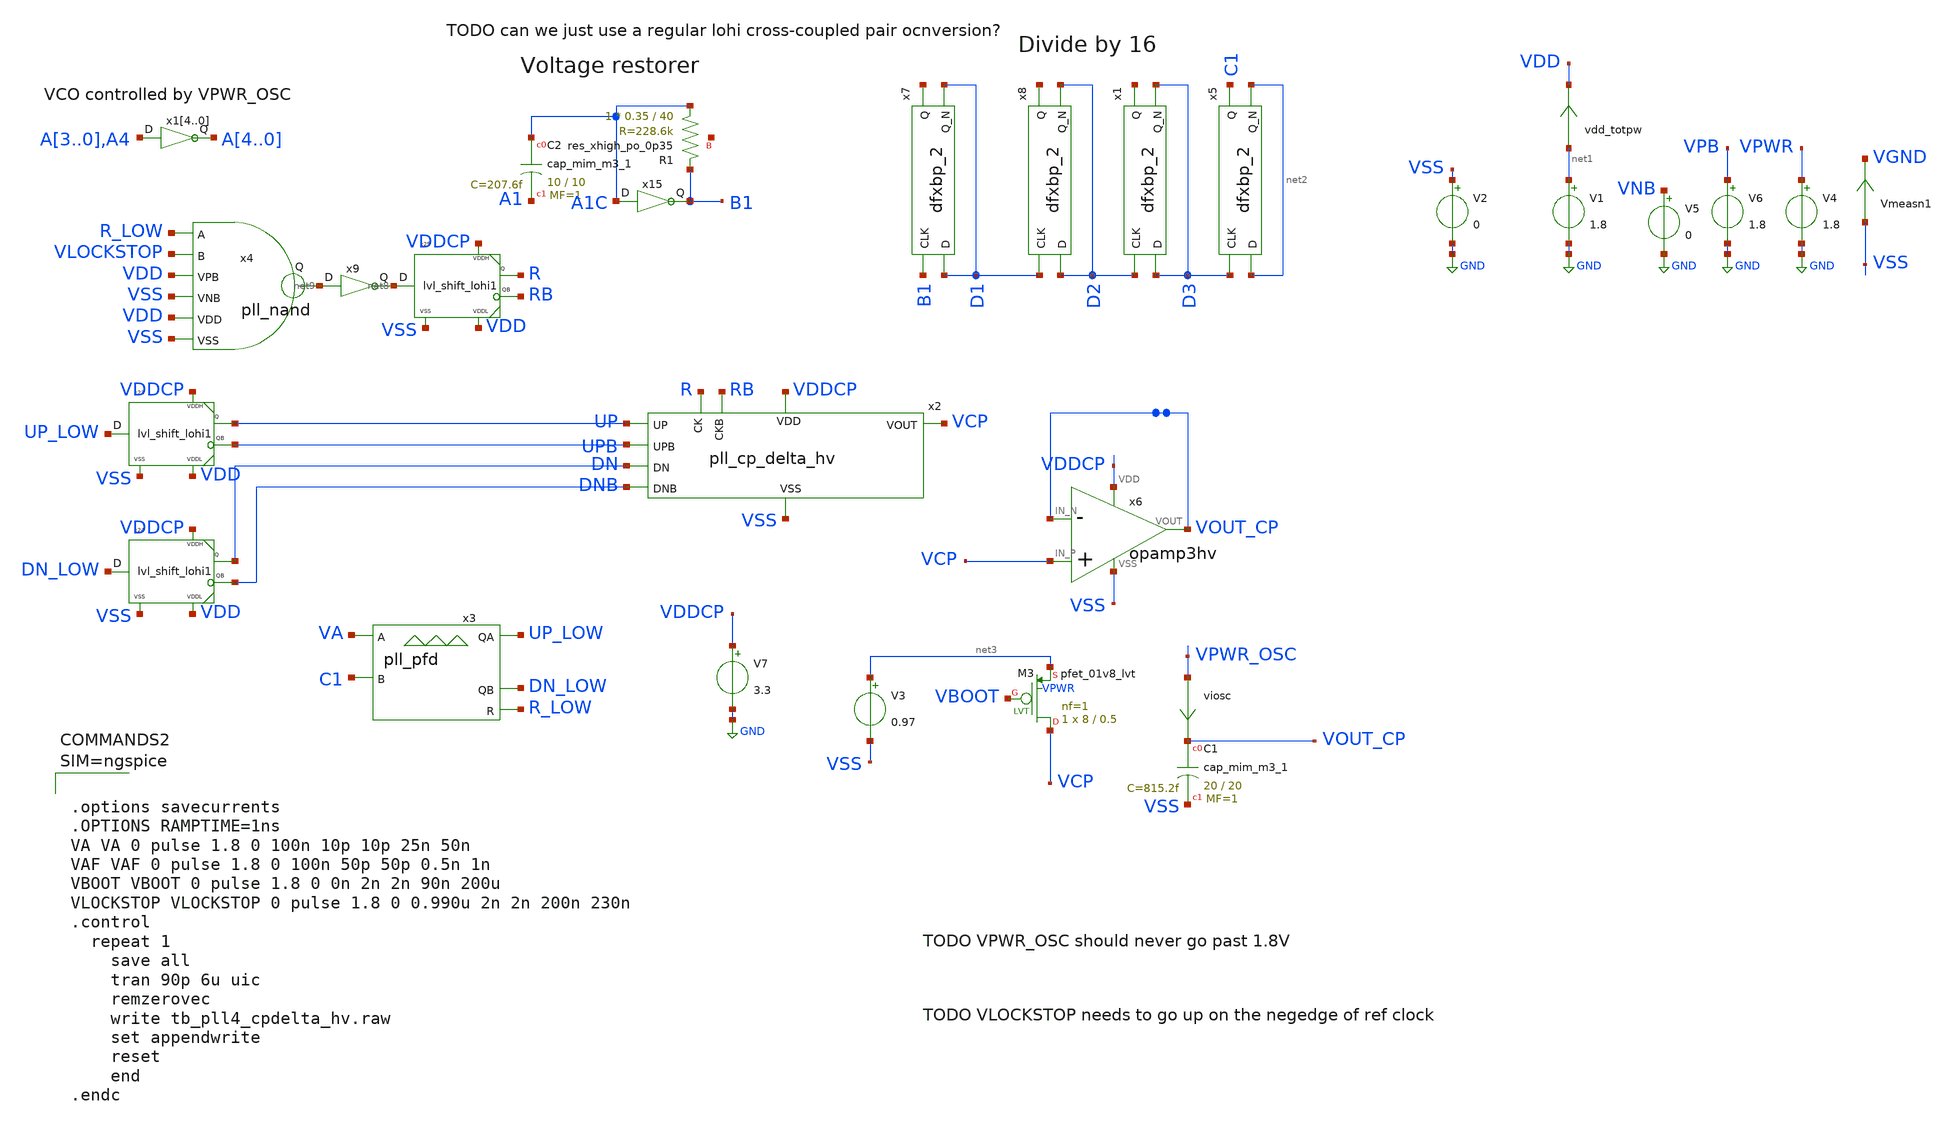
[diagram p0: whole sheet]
** sch_path: xschem/tb_pll4_cpdelta_hv.sch
**.subckt tb_pll4_cpdelta_hv
V5 VNB GND 0
V6 VPB GND 1.8
V1 net1 GND 1.8
V2 VSS GND 0
vdd_totpw net1 VDD 0
.save i(vdd_totpw)
Vmeasn1 VSS VGND 0
.save i(vmeasn1)
x3 VA C1 UP_LOW DN_LOW R_LOW VDD VSS pll_pfd
x7 B1 D1 VGND VNB VPB VPWR net4 D1 sky130_fd_sc_hd__dfxbp_2
x8 D1 D2 VGND VNB VPB VPWR net5 D2 sky130_fd_sc_hd__dfxbp_2
V4 VPWR GND 1.8
x1 D2 D3 VGND VNB VPB VPWR net6 D3 sky130_fd_sc_hd__dfxbp_2
x5 D3 net2 VGND VNB VPB VPWR C1 net2 sky130_fd_sc_hd__dfxbp_2
x14 A3 A4 VPWR_OSC VSS pll_inv1
x13 A2 A3 VPWR_OSC VSS pll_inv1
x12 A1 A2 VPWR_OSC VSS pll_inv1
x11 A0 A1 VPWR_OSC VSS pll_inv1
x10 A4 A0 VPWR_OSC VSS pll_inv1
V7 VDDCP GND 3.3
x15 A1C B1 VDD VSS pll_inv1
XR1 A1C B1 net7 sky130_fd_pr__res_xhigh_po_0p35 L=40 mult=1 m=1
XC2 A1C A1 sky130_fd_pr__cap_mim_m3_1 W=10 L=10 MF=1 m=1
viosc VPWR_OSC VOUT_CP 0
.save i(viosc)
V3 net3 VSS 0.97
x6 VDDCP VCP VOUT_CP VOUT_CP VSS opamp3hv
x2 VDDCP UP DN VCP VSS UPB DNB R RB pll_cp_delta_hv
x23 UP_LOW UP UPB VDDCP VDD VSS lvl_shift_lohi1
x24 DN_LOW DN DNB VDDCP VDD VSS lvl_shift_lohi1
x25 net8 R RB VDDCP VDD VSS lvl_shift_lohi1
x4 R_LOW VLOCKSTOP VDD VSS VDD VSS net9 pll_nand
x9 net9 net8 VDD VSS pll_inv1
XC1 VOUT_CP VSS sky130_fd_pr__cap_mim_m3_1 W=20 L=20 MF=1 m=1
XM3 VCP VBOOT net3 VPWR sky130_fd_pr__pfet_01v8_lvt L=0.5 W=8 nf=1 ad='int((nf+1)/2) * W/nf * 0.29' as='int((nf+2)/2) * W/nf * 0.29'
+ pd='2*int((nf+1)/2) * (W/nf + 0.29)' ps='2*int((nf+2)/2) * (W/nf + 0.29)' nrd='0.29 / W' nrs='0.29 / W'
+ sa=0 sb=0 sd=0 mult=1 m=1
**** begin user architecture code

** opencircuitdesign pdks install
.lib $::SKYWATER_MODELS/sky130.lib.spice tt_mm
.include $::SKYWATER_STDCELLS/sky130_fd_sc_hd.spice





.options savecurrents
.OPTIONS RAMPTIME=1ns
VA VA 0 pulse 1.8 0 100n 10p 10p 25n 50n
VAF VAF 0 pulse 1.8 0 100n 50p 50p 0.5n 1n
VBOOT VBOOT 0 pulse 1.8 0 0n 2n 2n 90n 200u
VLOCKSTOP VLOCKSTOP 0 pulse 1.8 0 0.990u 2n 2n 200n 230n
.control
  repeat 1
    save all
    tran 90p 6u uic
    remzerovec
    write tb_pll4_cpdelta_hv.raw
    set appendwrite
    reset
    end
.endc



**** end user architecture code
**.ends

* expanding   symbol:  pll_pfd.sym # of pins=5
** sym_path: xschem/pll_pfd.sym
** sch_path: xschem/pll_pfd.sch
.subckt pll_pfd A B QA QB R VDD VSS
*.ipin A
*.ipin B
*.iopin VDD
*.ipin VSS
*.opin QA
*.opin QB
*.opin R
x1 QA A QAB VDD VSS pll_nor
x2 QAB RA QA VDD VSS pll_nor
x3 QB B QBB VDD VSS pll_nor
x4 QBB RB QB VDD VSS pll_nor
x6 RAB QAB RA VDD VSS pll_nor
x7 RA R RAB VDD VSS pll_nor
x8 RBB QBB RB VDD VSS pll_nor
x9 RB R RBB VDD VSS pll_nor
x10 net2 net1 VDD VSS pll_inv1
x11 net3 net2 VDD VSS pll_inv1
x12 net1 R VDD VSS pll_inv1
x13 net1 R VDD VSS pll_inv1
x14 net1 R VDD VSS pll_inv1
x15 QB QA net3 VDD VSS pll_nand
.ends


* expanding   symbol:  pll_inv1.sym # of pins=2
** sym_path: xschem/pll_inv1.sym
** sch_path: xschem/pll_inv1.sch
.subckt pll_inv1 D Q VDD VSS
*.opin Q
*.ipin D
*.ipin VDD
*.ipin VSS
XM3 Q D net1 net1 sky130_fd_pr__pfet_01v8_lvt L=0.5 W=1 nf=1 ad='int((nf+1)/2) * W/nf * 0.29' as='int((nf+2)/2) * W/nf * 0.29'
+ pd='2*int((nf+1)/2) * (W/nf + 0.29)' ps='2*int((nf+2)/2) * (W/nf + 0.29)' nrd='0.29 / W' nrs='0.29 / W'
+ sa=0 sb=0 sd=0 mult=1 m=1
vpwr VDD net1 0
.save i(vpwr)
XM1 Q D VSS VSS sky130_fd_pr__nfet_01v8_lvt L=0.25 W=0.5 nf=1 ad='int((nf+1)/2) * W/nf * 0.29' as='int((nf+2)/2) * W/nf * 0.29'
+ pd='2*int((nf+1)/2) * (W/nf + 0.29)' ps='2*int((nf+2)/2) * (W/nf + 0.29)' nrd='0.29 / W' nrs='0.29 / W'
+ sa=0 sb=0 sd=0 mult=1 m=1
.ends


* expanding   symbol:  opamp3hv.sym # of pins=5
** sym_path: xschem/opamp3hv.sym
** sch_path: xschem/opamp3hv.sch
.subckt opamp3hv VDD IN_P IN_N VOUT VSS
*.iopin VDD
*.iopin VSS
*.ipin IN_N
*.opin VOUT
*.ipin IN_P
vimeasn net2 VN 0
.save i(vimeasn)
vimeasp net3 voutstage1 0
.save i(vimeasp)
vicom vcom net1 0
.save i(vicom)
V3 vbias VSS 1.2
XC1 VOUT voutstage1 sky130_fd_pr__cap_mim_m3_1 W=8 L=8 MF=1 m=1
XM6 net1 vbias VSS VSS sky130_fd_pr__nfet_g5v0d10v5 L=1 W=2 nf=1 ad='int((nf+1)/2) * W/nf * 0.29' as='int((nf+2)/2) * W/nf * 0.29'
+ pd='2*int((nf+1)/2) * (W/nf + 0.29)' ps='2*int((nf+2)/2) * (W/nf + 0.29)' nrd='0.29 / W' nrs='0.29 / W'
+ sa=0 sb=0 sd=0 mult=1 m=1
XM7 VN IN_N vcom VSS sky130_fd_pr__nfet_g5v0d10v5 L=1 W=2 nf=1 ad='int((nf+1)/2) * W/nf * 0.29' as='int((nf+2)/2) * W/nf * 0.29'
+ pd='2*int((nf+1)/2) * (W/nf + 0.29)' ps='2*int((nf+2)/2) * (W/nf + 0.29)' nrd='0.29 / W' nrs='0.29 / W'
+ sa=0 sb=0 sd=0 mult=1 m=1
XM8 net3 net2 VDD VDD sky130_fd_pr__pfet_g5v0d10v5 L=1 W=2 nf=1 ad='int((nf+1)/2) * W/nf * 0.29' as='int((nf+2)/2) * W/nf * 0.29'
+ pd='2*int((nf+1)/2) * (W/nf + 0.29)' ps='2*int((nf+2)/2) * (W/nf + 0.29)' nrd='0.29 / W' nrs='0.29 / W'
+ sa=0 sb=0 sd=0 mult=1 m=1
XM2 net2 net2 VDD VDD sky130_fd_pr__pfet_g5v0d10v5 L=1 W=2 nf=1 ad='int((nf+1)/2) * W/nf * 0.29' as='int((nf+2)/2) * W/nf * 0.29'
+ pd='2*int((nf+1)/2) * (W/nf + 0.29)' ps='2*int((nf+2)/2) * (W/nf + 0.29)' nrd='0.29 / W' nrs='0.29 / W'
+ sa=0 sb=0 sd=0 mult=1 m=1
XM1 VOUT voutstage1 VDD VDD sky130_fd_pr__pfet_g5v0d10v5 L=1 W=4 nf=1 ad='int((nf+1)/2) * W/nf * 0.29'
+ as='int((nf+2)/2) * W/nf * 0.29' pd='2*int((nf+1)/2) * (W/nf + 0.29)' ps='2*int((nf+2)/2) * (W/nf + 0.29)'
+ nrd='0.29 / W' nrs='0.29 / W' sa=0 sb=0 sd=0 mult=1 m=1
XM4 VOUT vbias VSS VSS sky130_fd_pr__nfet_g5v0d10v5 L=1 W=2 nf=1 ad='int((nf+1)/2) * W/nf * 0.29' as='int((nf+2)/2) * W/nf * 0.29'
+ pd='2*int((nf+1)/2) * (W/nf + 0.29)' ps='2*int((nf+2)/2) * (W/nf + 0.29)' nrd='0.29 / W' nrs='0.29 / W'
+ sa=0 sb=0 sd=0 mult=1 m=1
XM9 voutstage1 IN_P vcom VSS sky130_fd_pr__nfet_g5v0d10v5 L=1 W=2 nf=1 ad='int((nf+1)/2) * W/nf * 0.29'
+ as='int((nf+2)/2) * W/nf * 0.29' pd='2*int((nf+1)/2) * (W/nf + 0.29)' ps='2*int((nf+2)/2) * (W/nf + 0.29)'
+ nrd='0.29 / W' nrs='0.29 / W' sa=0 sb=0 sd=0 mult=1 m=1
.ends


* expanding   symbol:  pll_cp_delta_hv.sym # of pins=9
** sym_path: xschem/pll_cp_delta_hv.sym
** sch_path: xschem/pll_cp_delta_hv.sch
.subckt pll_cp_delta_hv VDD UP DN VOUT VSS UPB DNB CK CKB
*.opin VOUT
*.ipin VSS
*.ipin UP
*.ipin DNB
*.ipin CK
*.ipin CKB
*.ipin VDD
*.ipin DN
*.ipin UPB
*.ipin CK
vibias net3 net9 0
.save i(vibias)
XM16 net6 UPB VDD VDD sky130_fd_pr__pfet_g5v0d10v5 L=1 W=4 nf=1 ad='int((nf+1)/2) * W/nf * 0.29' as='int((nf+2)/2) * W/nf * 0.29'
+ pd='2*int((nf+1)/2) * (W/nf + 0.29)' ps='2*int((nf+2)/2) * (W/nf + 0.29)' nrd='0.29 / W' nrs='0.29 / W'
+ sa=0 sb=0 sd=0 mult=1 m=1
XM13 net2 VSS VDD VDD sky130_fd_pr__pfet_g5v0d10v5 L=1 W=4 nf=1 ad='int((nf+1)/2) * W/nf * 0.29' as='int((nf+2)/2) * W/nf * 0.29'
+ pd='2*int((nf+1)/2) * (W/nf + 0.29)' ps='2*int((nf+2)/2) * (W/nf + 0.29)' nrd='0.29 / W' nrs='0.29 / W'
+ sa=0 sb=0 sd=0 mult=1 m=1
XM14 net3 net3 net2 VDD sky130_fd_pr__pfet_g5v0d10v5 L=1 W=4 nf=1 ad='int((nf+1)/2) * W/nf * 0.29' as='int((nf+2)/2) * W/nf * 0.29'
+ pd='2*int((nf+1)/2) * (W/nf + 0.29)' ps='2*int((nf+2)/2) * (W/nf + 0.29)' nrd='0.29 / W' nrs='0.29 / W'
+ sa=0 sb=0 sd=0 mult=1 m=1
I0 VDD net4 10u
XM11 net1 VDD VSS VSS sky130_fd_pr__nfet_g5v0d10v5 L=1 W=2 nf=1 ad='int((nf+1)/2) * W/nf * 0.29' as='int((nf+2)/2) * W/nf * 0.29'
+ pd='2*int((nf+1)/2) * (W/nf + 0.29)' ps='2*int((nf+2)/2) * (W/nf + 0.29)' nrd='0.29 / W' nrs='0.29 / W'
+ sa=0 sb=0 sd=0 mult=1 m=1
XM17 net4 net4 net1 VSS sky130_fd_pr__nfet_g5v0d10v5 L=1 W=2 nf=1 ad='int((nf+1)/2) * W/nf * 0.29' as='int((nf+2)/2) * W/nf * 0.29'
+ pd='2*int((nf+1)/2) * (W/nf + 0.29)' ps='2*int((nf+2)/2) * (W/nf + 0.29)' nrd='0.29 / W' nrs='0.29 / W'
+ sa=0 sb=0 sd=0 mult=1 m=1
XM15 net5 VDD VSS VSS sky130_fd_pr__nfet_g5v0d10v5 L=1 W=2 nf=1 ad='int((nf+1)/2) * W/nf * 0.29' as='int((nf+2)/2) * W/nf * 0.29'
+ pd='2*int((nf+1)/2) * (W/nf + 0.29)' ps='2*int((nf+2)/2) * (W/nf + 0.29)' nrd='0.29 / W' nrs='0.29 / W'
+ sa=0 sb=0 sd=0 mult=1 m=1
XM18 net9 net4 net5 VSS sky130_fd_pr__nfet_g5v0d10v5 L=1 W=2 nf=1 ad='int((nf+1)/2) * W/nf * 0.29' as='int((nf+2)/2) * W/nf * 0.29'
+ pd='2*int((nf+1)/2) * (W/nf + 0.29)' ps='2*int((nf+2)/2) * (W/nf + 0.29)' nrd='0.29 / W' nrs='0.29 / W'
+ sa=0 sb=0 sd=0 mult=1 m=1
XM6 net7 DN VSS VSS sky130_fd_pr__nfet_g5v0d10v5 L=1 W=2 nf=1 ad='int((nf+1)/2) * W/nf * 0.29' as='int((nf+2)/2) * W/nf * 0.29'
+ pd='2*int((nf+1)/2) * (W/nf + 0.29)' ps='2*int((nf+2)/2) * (W/nf + 0.29)' nrd='0.29 / W' nrs='0.29 / W'
+ sa=0 sb=0 sd=0 mult=1 m=1
XM19 net8 net4 net7 VSS sky130_fd_pr__nfet_g5v0d10v5 L=1 W=2 nf=1 ad='int((nf+1)/2) * W/nf * 0.29' as='int((nf+2)/2) * W/nf * 0.29'
+ pd='2*int((nf+1)/2) * (W/nf + 0.29)' ps='2*int((nf+2)/2) * (W/nf + 0.29)' nrd='0.29 / W' nrs='0.29 / W'
+ sa=0 sb=0 sd=0 mult=1 m=1
XM4 net10 net3 net6 VDD sky130_fd_pr__pfet_g5v0d10v5 L=1 W=4 nf=1 ad='int((nf+1)/2) * W/nf * 0.29' as='int((nf+2)/2) * W/nf * 0.29'
+ pd='2*int((nf+1)/2) * (W/nf + 0.29)' ps='2*int((nf+2)/2) * (W/nf + 0.29)' nrd='0.29 / W' nrs='0.29 / W'
+ sa=0 sb=0 sd=0 mult=1 m=1
viup net10 VOUT 0
.save i(viup)
vidown VOUT net8 0
.save i(vidown)
XC3 VOUT VOUT sky130_fd_pr__cap_mim_m3_1 W=1 L=1 MF=1 m=1
XM3 VOUT CKB VOUT VDD sky130_fd_pr__pfet_01v8_lvt L=0.5 W=1 nf=1 ad='int((nf+1)/2) * W/nf * 0.29' as='int((nf+2)/2) * W/nf * 0.29'
+ pd='2*int((nf+1)/2) * (W/nf + 0.29)' ps='2*int((nf+2)/2) * (W/nf + 0.29)' nrd='0.29 / W' nrs='0.29 / W'
+ sa=0 sb=0 sd=0 mult=1 m=1
XM5 VOUT CK VOUT VSS sky130_fd_pr__nfet_01v8_lvt L=0.25 W=0.45 nf=1 ad='int((nf+1)/2) * W/nf * 0.29'
+ as='int((nf+2)/2) * W/nf * 0.29' pd='2*int((nf+1)/2) * (W/nf + 0.29)' ps='2*int((nf+2)/2) * (W/nf + 0.29)'
+ nrd='0.29 / W' nrs='0.29 / W' sa=0 sb=0 sd=0 mult=1 m=1
XC2 VOUT VSS sky130_fd_pr__cap_mim_m3_1 W=1500 L=150 MF=1 m=1
.ends


* expanding   symbol:  lvl_shift_lohi1.sym # of pins=6
** sym_path: xschem/lvl_shift_lohi1.sym
** sch_path: xschem/lvl_shift_lohi1.sch
.subckt lvl_shift_lohi1 D Q QB VDDH VDDL VSS
*.ipin D
*.opin Q
*.opin QB
*.iopin VDDH
*.iopin VDDL
*.iopin VSS
vpwr VDDL net1 0
.save i(vpwr)
XM1 QB Q VDDH VDDH sky130_fd_pr__pfet_g5v0d10v5 L=0.5 W=2 nf=1 ad='int((nf+1)/2) * W/nf * 0.29' as='int((nf+2)/2) * W/nf * 0.29'
+ pd='2*int((nf+1)/2) * (W/nf + 0.29)' ps='2*int((nf+2)/2) * (W/nf + 0.29)' nrd='0.29 / W' nrs='0.29 / W'
+ sa=0 sb=0 sd=0 mult=1 m=1
XM2 Q QB VDDH VDDH sky130_fd_pr__pfet_g5v0d10v5 L=0.5 W=2 nf=1 ad='int((nf+1)/2) * W/nf * 0.29' as='int((nf+2)/2) * W/nf * 0.29'
+ pd='2*int((nf+1)/2) * (W/nf + 0.29)' ps='2*int((nf+2)/2) * (W/nf + 0.29)' nrd='0.29 / W' nrs='0.29 / W'
+ sa=0 sb=0 sd=0 mult=1 m=1
XM3 QB D VSS VSS sky130_fd_pr__nfet_g5v0d10v5 L=0.5 W=4 nf=1 ad='int((nf+1)/2) * W/nf * 0.29' as='int((nf+2)/2) * W/nf * 0.29'
+ pd='2*int((nf+1)/2) * (W/nf + 0.29)' ps='2*int((nf+2)/2) * (W/nf + 0.29)' nrd='0.29 / W' nrs='0.29 / W'
+ sa=0 sb=0 sd=0 mult=1 m=1
XM4 Q DB VSS VSS sky130_fd_pr__nfet_g5v0d10v5 L=0.5 W=4 nf=1 ad='int((nf+1)/2) * W/nf * 0.29' as='int((nf+2)/2) * W/nf * 0.29'
+ pd='2*int((nf+1)/2) * (W/nf + 0.29)' ps='2*int((nf+2)/2) * (W/nf + 0.29)' nrd='0.29 / W' nrs='0.29 / W'
+ sa=0 sb=0 sd=0 mult=1 m=1
XM5 DB D VSS VSS sky130_fd_pr__nfet_01v8_lvt L=0.5 W=1 nf=1 ad='int((nf+1)/2) * W/nf * 0.29' as='int((nf+2)/2) * W/nf * 0.29'
+ pd='2*int((nf+1)/2) * (W/nf + 0.29)' ps='2*int((nf+2)/2) * (W/nf + 0.29)' nrd='0.29 / W' nrs='0.29 / W'
+ sa=0 sb=0 sd=0 mult=1 m=1
XM6 DB D net1 VDDL sky130_fd_pr__pfet_01v8_lvt L=0.5 W=2 nf=1 ad='int((nf+1)/2) * W/nf * 0.29' as='int((nf+2)/2) * W/nf * 0.29'
+ pd='2*int((nf+1)/2) * (W/nf + 0.29)' ps='2*int((nf+2)/2) * (W/nf + 0.29)' nrd='0.29 / W' nrs='0.29 / W'
+ sa=0 sb=0 sd=0 mult=1 m=1
.ends


* expanding   symbol:  pll_nand.sym # of pins=7
** sym_path: xschem/pll_nand.sym
** sch_path: xschem/pll_nand.sch
.subckt pll_nand A B VPB VNB VDD VSS Q
*.opin Q
*.ipin A
*.ipin B
*.ipin VDD
*.ipin VPB
*.ipin VNB
*.ipin VSS
XM3 Q B net2 VPB sky130_fd_pr__pfet_01v8_lvt L=0.35 W=1 nf=1 ad='int((nf+1)/2) * W/nf * 0.29' as='int((nf+2)/2) * W/nf * 0.29'
+ pd='2*int((nf+1)/2) * (W/nf + 0.29)' ps='2*int((nf+2)/2) * (W/nf + 0.29)' nrd='0.29 / W' nrs='0.29 / W'
+ sa=0 sb=0 sd=0 mult=1 m=1
vpwr VDD net2 0
.save i(vpwr)
XM1 net1 B VSS VNB sky130_fd_pr__nfet_01v8_lvt L=0.25 W=0.5 nf=1 ad='int((nf+1)/2) * W/nf * 0.29' as='int((nf+2)/2) * W/nf * 0.29'
+ pd='2*int((nf+1)/2) * (W/nf + 0.29)' ps='2*int((nf+2)/2) * (W/nf + 0.29)' nrd='0.29 / W' nrs='0.29 / W'
+ sa=0 sb=0 sd=0 mult=1 m=1
XM2 Q A net2 VPB sky130_fd_pr__pfet_01v8_lvt L=0.35 W=1 nf=1 ad='int((nf+1)/2) * W/nf * 0.29' as='int((nf+2)/2) * W/nf * 0.29'
+ pd='2*int((nf+1)/2) * (W/nf + 0.29)' ps='2*int((nf+2)/2) * (W/nf + 0.29)' nrd='0.29 / W' nrs='0.29 / W'
+ sa=0 sb=0 sd=0 mult=1 m=1
XM4 Q A net1 VNB sky130_fd_pr__nfet_01v8_lvt L=0.25 W=0.5 nf=1 ad='int((nf+1)/2) * W/nf * 0.29' as='int((nf+2)/2) * W/nf * 0.29'
+ pd='2*int((nf+1)/2) * (W/nf + 0.29)' ps='2*int((nf+2)/2) * (W/nf + 0.29)' nrd='0.29 / W' nrs='0.29 / W'
+ sa=0 sb=0 sd=0 mult=1 m=1
.ends


* expanding   symbol:  pll_nor.sym # of pins=3
** sym_path: xschem/pll_nor.sym
** sch_path: xschem/pll_nor.sch
.subckt pll_nor A B Q VDD VSS
*.opin Q
*.ipin A
*.ipin B
*.ipin VDD
*.ipin VSS
XM3 net1 A net2 net3 sky130_fd_pr__pfet_01v8_lvt L=0.35 W=1 nf=1 ad='int((nf+1)/2) * W/nf * 0.29' as='int((nf+2)/2) * W/nf * 0.29'
+ pd='2*int((nf+1)/2) * (W/nf + 0.29)' ps='2*int((nf+2)/2) * (W/nf + 0.29)' nrd='0.29 / W' nrs='0.29 / W'
+ sa=0 sb=0 sd=0 mult=1 m=1
vpwr VDD net2 0
.save i(vpwr)
XM1 Q A VSS VSS sky130_fd_pr__nfet_01v8_lvt L=0.25 W=0.5 nf=1 ad='int((nf+1)/2) * W/nf * 0.29' as='int((nf+2)/2) * W/nf * 0.29'
+ pd='2*int((nf+1)/2) * (W/nf + 0.29)' ps='2*int((nf+2)/2) * (W/nf + 0.29)' nrd='0.29 / W' nrs='0.29 / W'
+ sa=0 sb=0 sd=0 mult=1 m=1
XM2 Q B net1 net2 sky130_fd_pr__pfet_01v8_lvt L=0.35 W=1 nf=1 ad='int((nf+1)/2) * W/nf * 0.29' as='int((nf+2)/2) * W/nf * 0.29'
+ pd='2*int((nf+1)/2) * (W/nf + 0.29)' ps='2*int((nf+2)/2) * (W/nf + 0.29)' nrd='0.29 / W' nrs='0.29 / W'
+ sa=0 sb=0 sd=0 mult=1 m=1
XM4 Q B VSS VSS sky130_fd_pr__nfet_01v8_lvt L=0.25 W=0.5 nf=1 ad='int((nf+1)/2) * W/nf * 0.29' as='int((nf+2)/2) * W/nf * 0.29'
+ pd='2*int((nf+1)/2) * (W/nf + 0.29)' ps='2*int((nf+2)/2) * (W/nf + 0.29)' nrd='0.29 / W' nrs='0.29 / W'
+ sa=0 sb=0 sd=0 mult=1 m=1
.ends

.GLOBAL GND
.end
